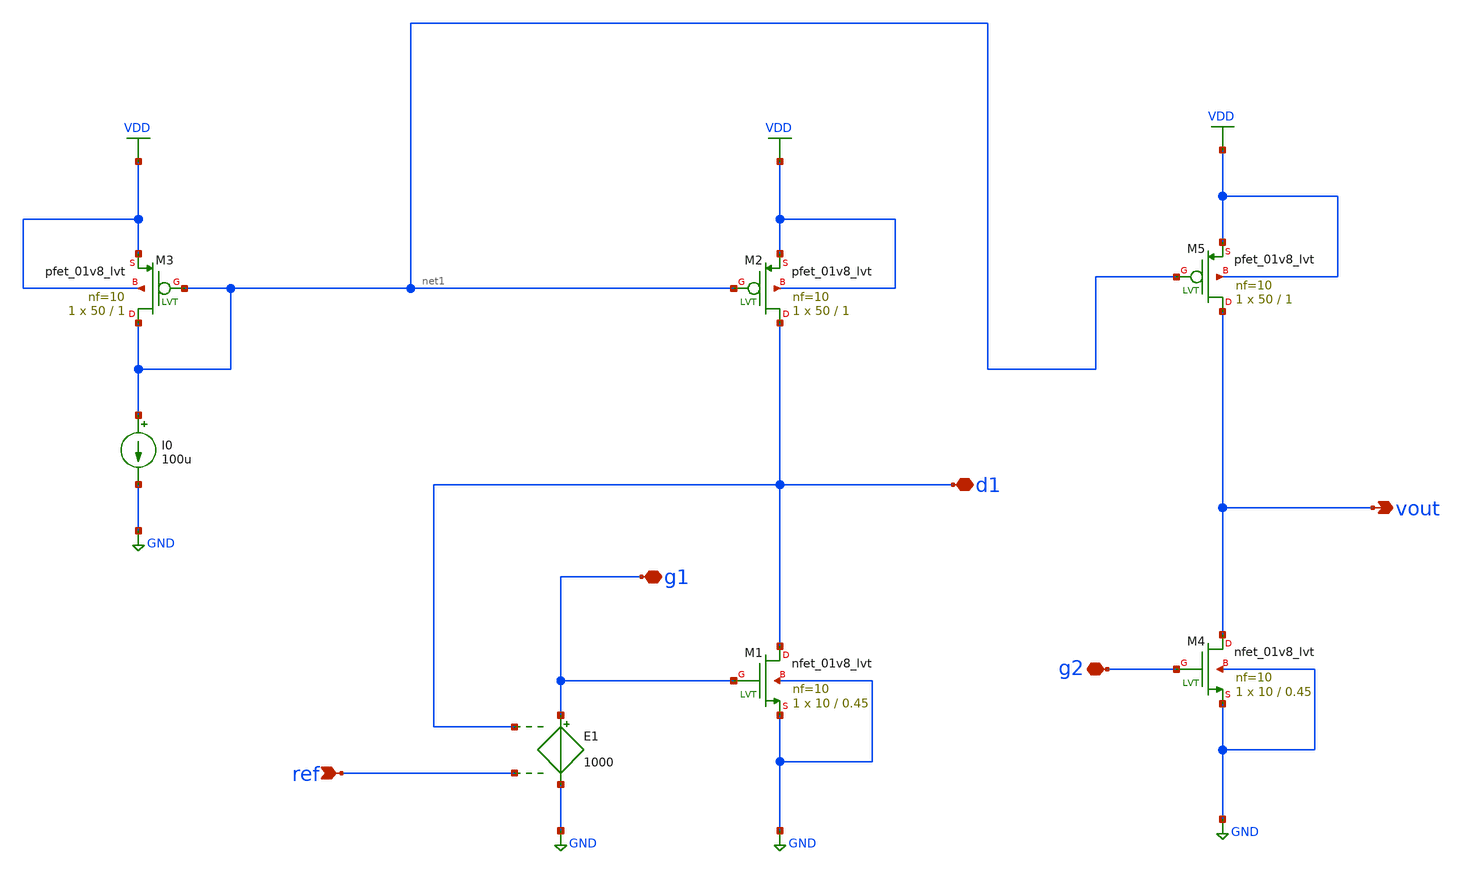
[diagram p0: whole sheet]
** sch_path: SelfStudy/Analog/Tony Chan/SpiceSim/cs-amp-gain-lvt.sch
**.subckt cs-amp-gain-lvt d1 ref g1 g2 vout
*.iopin d1
*.ipin ref
*.iopin g1
*.iopin g2
*.opin vout
I0 net1 GND 100u
E1 g1 GND d1 ref 1000
XM1 d1 g1 GND GND sky130_fd_pr__nfet_01v8_lvt L=0.45 W=10 nf=10 ad='int((nf+1)/2) * W/nf * 0.29' as='int((nf+2)/2) * W/nf * 0.29'
+ pd='2*int((nf+1)/2) * (W/nf + 0.29)' ps='2*int((nf+2)/2) * (W/nf + 0.29)' nrd='0.29 / W' nrs='0.29 / W'
+ sa=0 sb=0 sd=0 mult=1 m=1
XM2 d1 net1 VDD VDD sky130_fd_pr__pfet_01v8_lvt L=1 W=50 nf=10 ad='int((nf+1)/2) * W/nf * 0.29' as='int((nf+2)/2) * W/nf * 0.29'
+ pd='2*int((nf+1)/2) * (W/nf + 0.29)' ps='2*int((nf+2)/2) * (W/nf + 0.29)' nrd='0.29 / W' nrs='0.29 / W'
+ sa=0 sb=0 sd=0 mult=1 m=1
XM3 net1 net1 VDD VDD sky130_fd_pr__pfet_01v8_lvt L=1 W=50 nf=10 ad='int((nf+1)/2) * W/nf * 0.29' as='int((nf+2)/2) * W/nf * 0.29'
+ pd='2*int((nf+1)/2) * (W/nf + 0.29)' ps='2*int((nf+2)/2) * (W/nf + 0.29)' nrd='0.29 / W' nrs='0.29 / W'
+ sa=0 sb=0 sd=0 mult=1 m=1
XM4 vout g2 GND GND sky130_fd_pr__nfet_01v8_lvt L=0.45 W=10 nf=10 ad='int((nf+1)/2) * W/nf * 0.29' as='int((nf+2)/2) * W/nf * 0.29'
+ pd='2*int((nf+1)/2) * (W/nf + 0.29)' ps='2*int((nf+2)/2) * (W/nf + 0.29)' nrd='0.29 / W' nrs='0.29 / W'
+ sa=0 sb=0 sd=0 mult=1 m=1
XM5 vout net1 VDD VDD sky130_fd_pr__pfet_01v8_lvt L=1 W=50 nf=10 ad='int((nf+1)/2) * W/nf * 0.29' as='int((nf+2)/2) * W/nf * 0.29'
+ pd='2*int((nf+1)/2) * (W/nf + 0.29)' ps='2*int((nf+2)/2) * (W/nf + 0.29)' nrd='0.29 / W' nrs='0.29 / W'
+ sa=0 sb=0 sd=0 mult=1 m=1
**** begin user architecture code


.lib /usr/local/share/pdk/sky130A/libs.tech/ngspice/sky130.lib.spice tt
.option wnflag = 1

vds ref 0 0.9
vsup VDD 0 1.8
vin g1 g2 dc=0 ac=1

*cinf bias1 0 1n
*cload vout 0 100f

.control
save all

save @m.xm4.msky130_fd_pr__nfet_01v8_lvt[gm]
save @m.xm4.msky130_fd_pr__nfet_01v8_lvt[id]
save @m.xm4.msky130_fd_pr__nfet_01v8_lvt[gds]

save @m.xm5.msky130_fd_pr__pfet_01v8_lvt[gm]
save @m.xm5.msky130_fd_pr__pfet_01v8_lvt[id]
save @m.xm5.msky130_fd_pr__pfet_01v8_lvt[gds]

dc vin -1 1 0.001

let gdsn = @m.xm4.msky130_fd_pr__nfet_01v8_lvt[gds]
let gdsp = @m.xm5.msky130_fd_pr__pfet_01v8_lvt[gds]

let gmn = @m.xm4.msky130_fd_pr__nfet_01v8_lvt[gm]
let idn = @m.xm4.msky130_fd_pr__nfet_01v8_lvt[id]

let gmp = @m.xm5.msky130_fd_pr__pfet_01v8_lvt[gm]
let idp = @m.xm5.msky130_fd_pr__pfet_01v8_lvt[id]

let gmoveridn = gmn / idn
let vovn = 2 * idn / gmn

let gmoveridp = gmp / idp
let vovp = 2 * idp / gmp

let ao = gmn / (gdsn + gdsp)

plot v(vout)
plot deriv(v(vout)) vs v(vout) ao vs v(vout)
plot gmoveridn vs v(vout) gmoveridp vs v(vout)
plot vovn vs v(vout) vovp vs v(vout)

* Save DC sweep results
setplot dc1
write dc.raw

ac dec 100 1 1T
plot  v(g2) vdb(vout)

* Save AC response
setplot ac1
write ac.raw

set sqrnoise
noise v(vout) vin dec 100 1 1T

* Save noise spectrum (this is what you want to view)
setplot noise1
plot 10*log10(onoise_spectrum)
write noise.raw

* Save integrated noise result separately
setplot noise2
print onoise_total
write integrated_noise.raw

.endc


**** end user architecture code
**.ends
.GLOBAL GND
.GLOBAL VDD
.end
